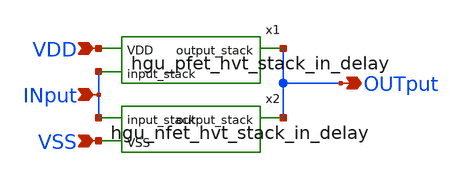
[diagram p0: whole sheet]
** sch_path: hgu/mag/delay_cell/5n_delay_cell/stack_test_inv.sch
**.subckt stack_test_inv INput VDD VSS OUTput
*.ipin INput
*.ipin VDD
*.ipin VSS
*.opin OUTput
x1 VDD INput OUTput hgu_pfet_hvt_stack_in_delay
x2 INput OUTput VSS hgu_nfet_hvt_stack_in_delay
**.ends

* expanding   symbol:  /foss/designs/hgu_goss/hgu/xschem/hgu_pfet_hvt_stack_in_delay.sym # of pins=3
** sym_path: hgu/xschem/hgu_pfet_hvt_stack_in_delay.sym
** sch_path: hgu/xschem/hgu_pfet_hvt_stack_in_delay.sch
.subckt hgu_pfet_hvt_stack_in_delay VDD input_stack output_stack
*.ipin VDD
*.ipin input_stack
*.iopin output_stack
XM1 output_stack input_stack net1 VDD sky130_fd_pr__pfet_01v8_hvt L=0.15 W=0.42 nf=1 ad='int((nf+1)/2) * W/nf * 0.29'
+ as='int((nf+2)/2) * W/nf * 0.29' pd='2*int((nf+1)/2) * (W/nf + 0.29)' ps='2*int((nf+2)/2) * (W/nf + 0.29)'
+ nrd='0.29 / W' nrs='0.29 / W' sa=0 sb=0 sd=0 mult=1 m=1
XM2 net1 input_stack net2 VDD sky130_fd_pr__pfet_01v8_hvt L=0.15 W=0.43 nf=1 ad='int((nf+1)/2) * W/nf * 0.29'
+ as='int((nf+2)/2) * W/nf * 0.29' pd='2*int((nf+1)/2) * (W/nf + 0.29)' ps='2*int((nf+2)/2) * (W/nf + 0.29)'
+ nrd='0.29 / W' nrs='0.29 / W' sa=0 sb=0 sd=0 mult=1 m=1
XM3 net2 input_stack VDD VDD sky130_fd_pr__pfet_01v8_hvt L=0.15 W=0.43 nf=1 ad='int((nf+1)/2) * W/nf * 0.29'
+ as='int((nf+2)/2) * W/nf * 0.29' pd='2*int((nf+1)/2) * (W/nf + 0.29)' ps='2*int((nf+2)/2) * (W/nf + 0.29)'
+ nrd='0.29 / W' nrs='0.29 / W' sa=0 sb=0 sd=0 mult=1 m=1
.ends


* expanding   symbol:  /foss/designs/hgu_goss/hgu/xschem/hgu_nfet_hvt_stack_in_delay.sym # of pins=3
** sym_path: hgu/xschem/hgu_nfet_hvt_stack_in_delay.sym
** sch_path: hgu/xschem/hgu_nfet_hvt_stack_in_delay.sch
.subckt hgu_nfet_hvt_stack_in_delay input_stack output_stack VSS
*.ipin VSS
*.ipin input_stack
*.iopin output_stack
XM1 output_stack input_stack net1 VSS sky130_fd_pr__nfet_01v8 L=0.15 W=0.42 nf=1 ad='int((nf+1)/2) * W/nf * 0.29'
+ as='int((nf+2)/2) * W/nf * 0.29' pd='2*int((nf+1)/2) * (W/nf + 0.29)' ps='2*int((nf+2)/2) * (W/nf + 0.29)'
+ nrd='0.29 / W' nrs='0.29 / W' sa=0 sb=0 sd=0 mult=1 m=1
XM2 net1 input_stack net2 VSS sky130_fd_pr__nfet_01v8 L=0.15 W=0.42 nf=1 ad='int((nf+1)/2) * W/nf * 0.29'
+ as='int((nf+2)/2) * W/nf * 0.29' pd='2*int((nf+1)/2) * (W/nf + 0.29)' ps='2*int((nf+2)/2) * (W/nf + 0.29)'
+ nrd='0.29 / W' nrs='0.29 / W' sa=0 sb=0 sd=0 mult=1 m=1
XM3 net2 input_stack net3 VSS sky130_fd_pr__nfet_01v8 L=0.15 W=0.42 nf=1 ad='int((nf+1)/2) * W/nf * 0.29'
+ as='int((nf+2)/2) * W/nf * 0.29' pd='2*int((nf+1)/2) * (W/nf + 0.29)' ps='2*int((nf+2)/2) * (W/nf + 0.29)'
+ nrd='0.29 / W' nrs='0.29 / W' sa=0 sb=0 sd=0 mult=1 m=1
XM4 net3 input_stack net4 VSS sky130_fd_pr__nfet_01v8 L=0.15 W=0.42 nf=1 ad='int((nf+1)/2) * W/nf * 0.29'
+ as='int((nf+2)/2) * W/nf * 0.29' pd='2*int((nf+1)/2) * (W/nf + 0.29)' ps='2*int((nf+2)/2) * (W/nf + 0.29)'
+ nrd='0.29 / W' nrs='0.29 / W' sa=0 sb=0 sd=0 mult=1 m=1
XM5 net4 input_stack net5 VSS sky130_fd_pr__nfet_01v8 L=0.15 W=0.42 nf=1 ad='int((nf+1)/2) * W/nf * 0.29'
+ as='int((nf+2)/2) * W/nf * 0.29' pd='2*int((nf+1)/2) * (W/nf + 0.29)' ps='2*int((nf+2)/2) * (W/nf + 0.29)'
+ nrd='0.29 / W' nrs='0.29 / W' sa=0 sb=0 sd=0 mult=1 m=1
XM6 net5 input_stack net6 VSS sky130_fd_pr__nfet_01v8 L=0.15 W=0.42 nf=1 ad='int((nf+1)/2) * W/nf * 0.29'
+ as='int((nf+2)/2) * W/nf * 0.29' pd='2*int((nf+1)/2) * (W/nf + 0.29)' ps='2*int((nf+2)/2) * (W/nf + 0.29)'
+ nrd='0.29 / W' nrs='0.29 / W' sa=0 sb=0 sd=0 mult=1 m=1
XM7 net6 input_stack net7 VSS sky130_fd_pr__nfet_01v8 L=0.15 W=0.42 nf=1 ad='int((nf+1)/2) * W/nf * 0.29'
+ as='int((nf+2)/2) * W/nf * 0.29' pd='2*int((nf+1)/2) * (W/nf + 0.29)' ps='2*int((nf+2)/2) * (W/nf + 0.29)'
+ nrd='0.29 / W' nrs='0.29 / W' sa=0 sb=0 sd=0 mult=1 m=1
XM8 net7 input_stack net8 VSS sky130_fd_pr__nfet_01v8 L=0.15 W=0.42 nf=1 ad='int((nf+1)/2) * W/nf * 0.29'
+ as='int((nf+2)/2) * W/nf * 0.29' pd='2*int((nf+1)/2) * (W/nf + 0.29)' ps='2*int((nf+2)/2) * (W/nf + 0.29)'
+ nrd='0.29 / W' nrs='0.29 / W' sa=0 sb=0 sd=0 mult=1 m=1
XM9 net8 input_stack net9 VSS sky130_fd_pr__nfet_01v8 L=0.15 W=0.42 nf=1 ad='int((nf+1)/2) * W/nf * 0.29'
+ as='int((nf+2)/2) * W/nf * 0.29' pd='2*int((nf+1)/2) * (W/nf + 0.29)' ps='2*int((nf+2)/2) * (W/nf + 0.29)'
+ nrd='0.29 / W' nrs='0.29 / W' sa=0 sb=0 sd=0 mult=1 m=1
XM10 net9 input_stack net10 VSS sky130_fd_pr__nfet_01v8 L=0.15 W=0.42 nf=1 ad='int((nf+1)/2) * W/nf * 0.29'
+ as='int((nf+2)/2) * W/nf * 0.29' pd='2*int((nf+1)/2) * (W/nf + 0.29)' ps='2*int((nf+2)/2) * (W/nf + 0.29)'
+ nrd='0.29 / W' nrs='0.29 / W' sa=0 sb=0 sd=0 mult=1 m=1
XM11 net10 input_stack net11 VSS sky130_fd_pr__nfet_01v8 L=0.15 W=0.42 nf=1 ad='int((nf+1)/2) * W/nf * 0.29'
+ as='int((nf+2)/2) * W/nf * 0.29' pd='2*int((nf+1)/2) * (W/nf + 0.29)' ps='2*int((nf+2)/2) * (W/nf + 0.29)'
+ nrd='0.29 / W' nrs='0.29 / W' sa=0 sb=0 sd=0 mult=1 m=1
XM12 net11 input_stack net12 VSS sky130_fd_pr__nfet_01v8 L=0.15 W=0.42 nf=1 ad='int((nf+1)/2) * W/nf * 0.29'
+ as='int((nf+2)/2) * W/nf * 0.29' pd='2*int((nf+1)/2) * (W/nf + 0.29)' ps='2*int((nf+2)/2) * (W/nf + 0.29)'
+ nrd='0.29 / W' nrs='0.29 / W' sa=0 sb=0 sd=0 mult=1 m=1
XM13 net12 input_stack net13 VSS sky130_fd_pr__nfet_01v8 L=0.15 W=0.42 nf=1 ad='int((nf+1)/2) * W/nf * 0.29'
+ as='int((nf+2)/2) * W/nf * 0.29' pd='2*int((nf+1)/2) * (W/nf + 0.29)' ps='2*int((nf+2)/2) * (W/nf + 0.29)'
+ nrd='0.29 / W' nrs='0.29 / W' sa=0 sb=0 sd=0 mult=1 m=1
XM14 net13 input_stack net14 VSS sky130_fd_pr__nfet_01v8 L=0.15 W=0.42 nf=1 ad='int((nf+1)/2) * W/nf * 0.29'
+ as='int((nf+2)/2) * W/nf * 0.29' pd='2*int((nf+1)/2) * (W/nf + 0.29)' ps='2*int((nf+2)/2) * (W/nf + 0.29)'
+ nrd='0.29 / W' nrs='0.29 / W' sa=0 sb=0 sd=0 mult=1 m=1
XM15 net14 input_stack net15 VSS sky130_fd_pr__nfet_01v8 L=0.15 W=0.42 nf=1 ad='int((nf+1)/2) * W/nf * 0.29'
+ as='int((nf+2)/2) * W/nf * 0.29' pd='2*int((nf+1)/2) * (W/nf + 0.29)' ps='2*int((nf+2)/2) * (W/nf + 0.29)'
+ nrd='0.29 / W' nrs='0.29 / W' sa=0 sb=0 sd=0 mult=1 m=1
XM16 net15 input_stack VSS VSS sky130_fd_pr__nfet_01v8 L=0.15 W=0.42 nf=1 ad='int((nf+1)/2) * W/nf * 0.29'
+ as='int((nf+2)/2) * W/nf * 0.29' pd='2*int((nf+1)/2) * (W/nf + 0.29)' ps='2*int((nf+2)/2) * (W/nf + 0.29)'
+ nrd='0.29 / W' nrs='0.29 / W' sa=0 sb=0 sd=0 mult=1 m=1
.ends

.end
